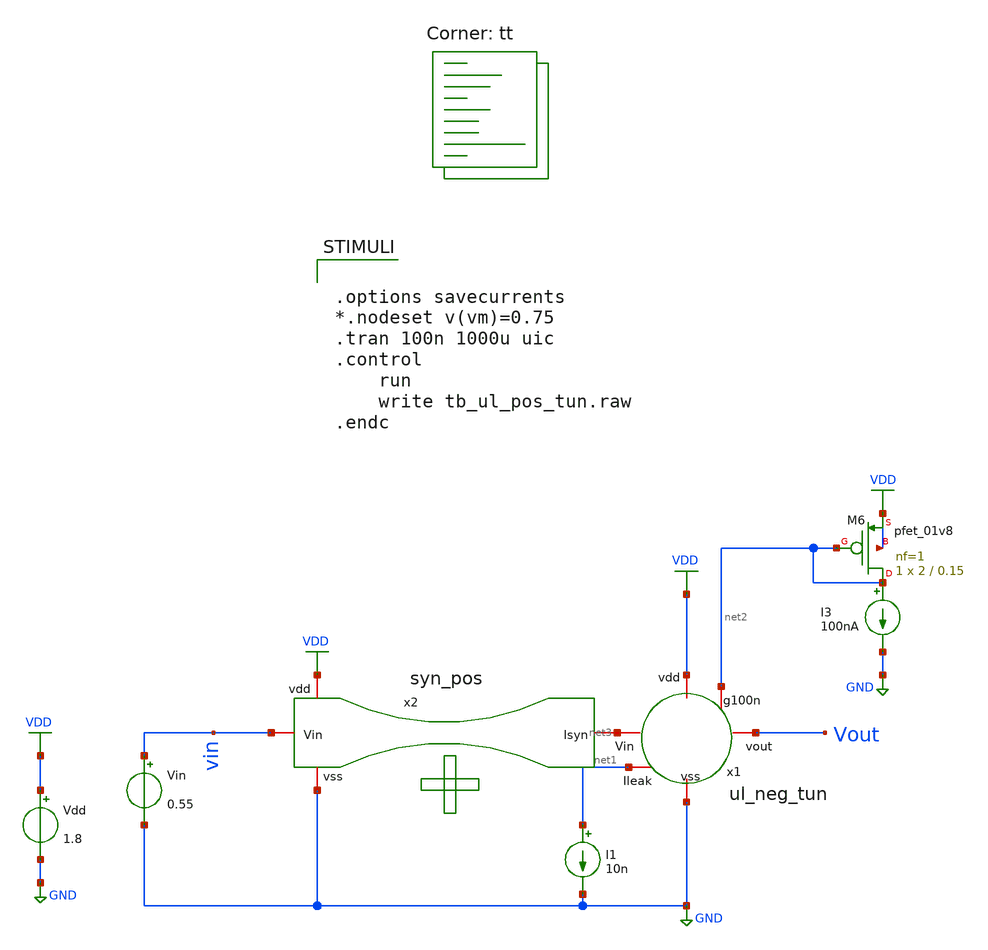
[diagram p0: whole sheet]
** sch_path: Neuron/ultralif/tb_ul_pos_tun.sch
**.subckt tb_ul_pos_tun
I1 net1 GND 10n
Vdd VDD GND 1.8
I3 net2 GND 100nA
Vin vin GND 0.55
XM6 net2 net2 VDD VDD sky130_fd_pr__pfet_01v8 L=0.15 W=2 nf=1 ad='int((nf+1)/2) * W/nf * 0.29' as='int((nf+2)/2) * W/nf * 0.29'
+ pd='2*int((nf+1)/2) * (W/nf + 0.29)' ps='2*int((nf+2)/2) * (W/nf + 0.29)' nrd='0.29 / W' nrs='0.29 / W'
+ sa=0 sb=0 sd=0 mult=1 m=1
x1 net3 VDD net2 Vout net1 GND ul_neg_tun
x2 GND vin net3 VDD syn_pos
**** begin user architecture code
.lib $::SKYWATER_MODELS/sky130.lib.spice tt
**** end user architecture code
**.ends
.GLOBAL GND
.GLOBAL VDD
**** begin user architecture code


.options savecurrents
*.nodeset v(vm)=0.75
.tran 100n 1000u uic
.control
	run
	write tb_ul_pos_tun.raw
.endc


**** end user architecture code
.end
